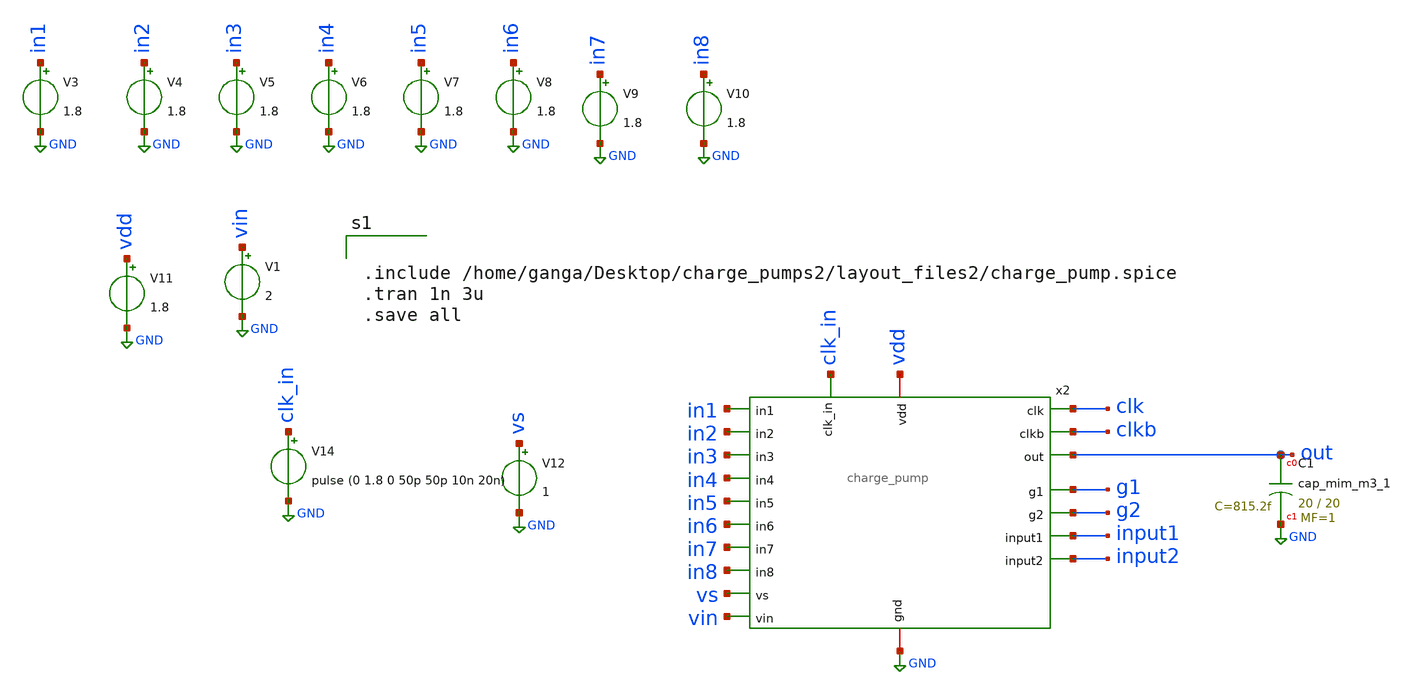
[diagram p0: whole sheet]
** sch_path: xschem/charge_pump_tb.sch
**.subckt charge_pump_tb
V1 vin GND 2
V3 in1 GND 1.8
V4 in2 GND 1.8
V5 in3 GND 1.8
V6 in4 GND 1.8
V7 in5 GND 1.8
V8 in6 GND 1.8
V9 in7 GND 1.8
V10 in8 GND 1.8
V11 vdd GND 1.8
V12 vs GND 1
XC1 out GND sky130_fd_pr__cap_mim_m3_1 W=20 L=20 MF=1 m=1
V14 clk_in GND pulse (0 1.8 0 50p 50p 10n 20n)
x2 vin vs in1 in2 in3 in4 in5 in6 in7 in8 input1 input2 out clk clkb clk_in g1 g2 GND vdd
+ charge_pump
**** begin user architecture code

** opencircuitdesign pdks install
.lib $::SKYWATER_MODELS/sky130.lib.spice tt




.include /home/ganga/Desktop/charge_pumps2/layout_files2/charge_pump.spice
.tran 1n 3u
.save all


**** end user architecture code
**.ends
.GLOBAL GND
.end
